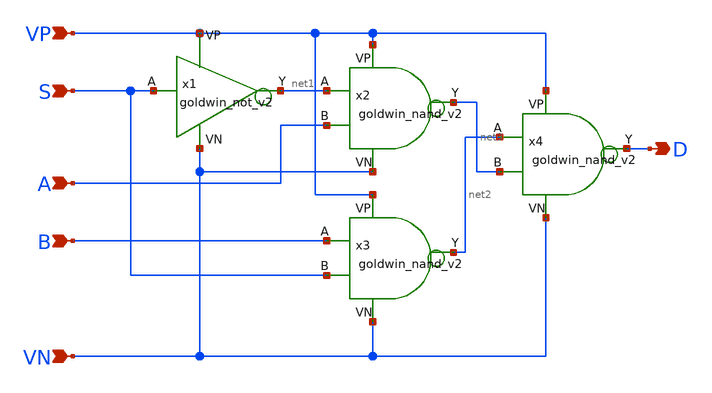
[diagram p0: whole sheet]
** sch_path: APIC-UTS/schematic/goldwin_mux_v2/goldwin_mux_v2.sch
**.subckt goldwin_mux_v2 A B S VP VN D
*.ipin A
*.ipin B
*.ipin S
*.ipin VP
*.ipin VN
*.opin D
x1 S net1 VP VN goldwin_not_v2
x2 net1 A net3 VP VN goldwin_nand_v2
x3 B S net2 VP VN goldwin_nand_v2
x4 net2 net3 D VP VN goldwin_nand_v2
**.ends
.end
